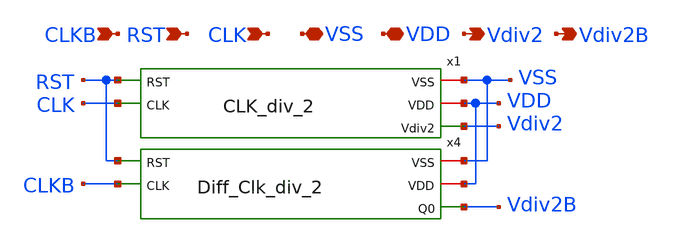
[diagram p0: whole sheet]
** sch_path: Clock_Generator_PAKISTAN_02/Schematics/DIFFER_CLK_div_2.sch
**.subckt DIFFER_CLK_div_2 CLK VSS VDD RST Vdiv2 Vdiv2B CLKB
*.ipin CLK
*.iopin VSS
*.iopin VDD
*.ipin RST
*.opin Vdiv2
*.opin Vdiv2B
*.ipin CLKB
x1 VSS VDD Vdiv2 RST CLK CLK_div_2
x4 VSS VDD Vdiv2B RST CLKB Diff_Clk_div_2
**.ends
.end
